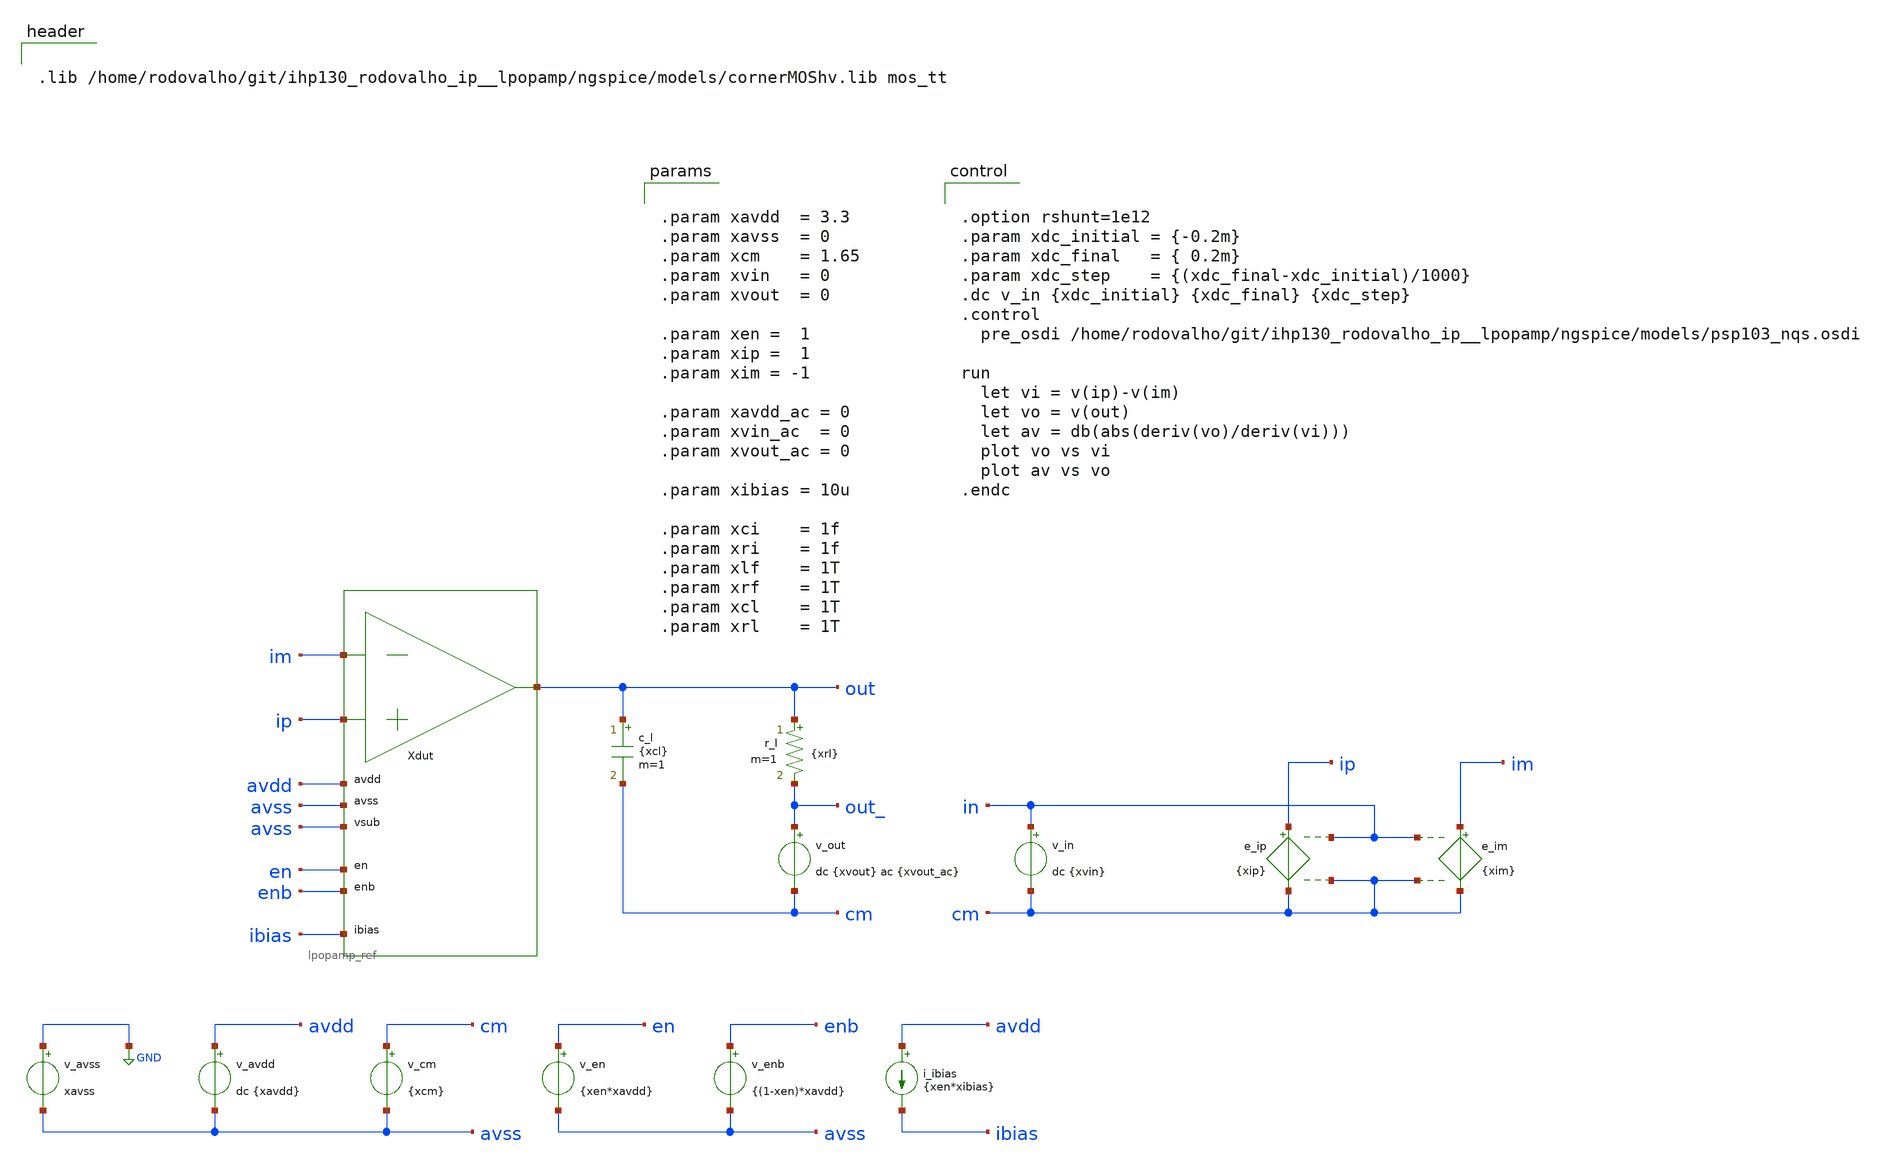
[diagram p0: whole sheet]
** sch_path: xschem/tb_lpopamp_open_dc.sch
**.subckt tb_lpopamp_open_dc
Xdut im ip out avdd avss avss en enb ibias lpopamp_ref
v_avss GND avss xavss
v_avdd avdd avss dc {xavdd}
v_in in cm dc {xvin}
v_en en avss {xen*xavdd}
v_enb enb avss {(1-xen)*xavdd}
i_ibias avdd ibias {xen*xibias}
c_l out cm {xcl} m=1
v_out out_ cm dc {xvout} ac {xvout_ac}
r_l out out_ {xrl} m=1
e_ip ip cm in cm {xip}
e_im im cm in cm {xim}
v_cm cm avss {xcm}
**** begin user architecture code


.lib /home/rodovalho/git/ihp130_rodovalho_ip__lpopamp/ngspice/models/cornerMOShv.lib mos_tt




.option rshunt=1e12
.param xdc_initial = {-0.2m}
.param xdc_final   = { 0.2m}
.param xdc_step    = {(xdc_final-xdc_initial)/1000}
.dc v_in {xdc_initial} {xdc_final} {xdc_step}
.control
  pre_osdi /home/rodovalho/git/ihp130_rodovalho_ip__lpopamp/ngspice/models/psp103_nqs.osdi

run
  let vi = v(ip)-v(im)
  let vo = v(out)
  let av = db(abs(deriv(vo)/deriv(vi)))
  plot vo vs vi
  plot av vs vo
.endc




.param xavdd  = 3.3
.param xavss  = 0
.param xcm    = 1.65
.param xvin   = 0
.param xvout  = 0

.param xen =  1
.param xip =  1
.param xim = -1

.param xavdd_ac = 0
.param xvin_ac  = 0
.param xvout_ac = 0

.param xibias = 10u

.param xci    = 1f
.param xri    = 1f
.param xlf    = 1T
.param xrf    = 1T
.param xcl    = 1T
.param xrl    = 1T


**** end user architecture code
**.ends
.GLOBAL GND
.end
